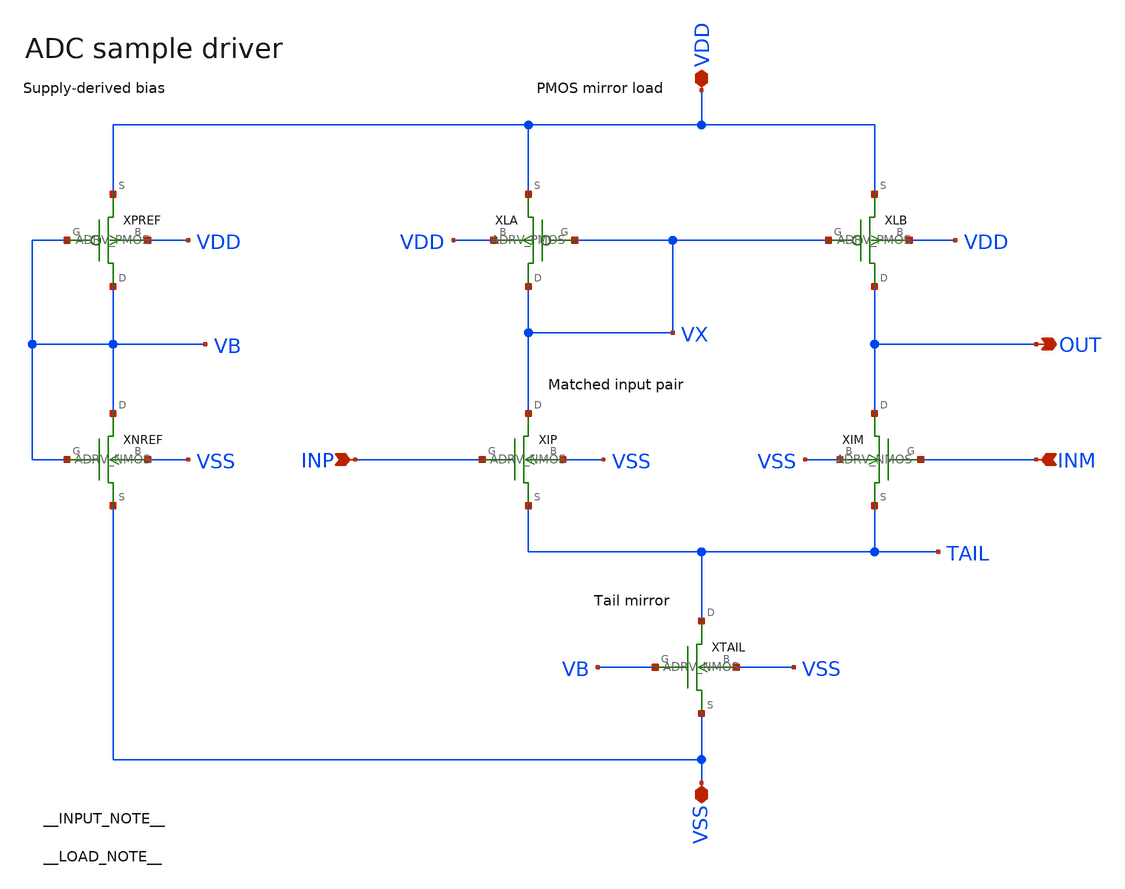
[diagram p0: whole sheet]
** sch_path: examples/sky130-adc-driver/ADRV_OTA.sch
**.subckt ADRV_OTA VDD VSS INP INM OUT
*.iopin VDD
*.iopin VSS
*.ipin INP
*.ipin INM
*.opin OUT
XPREF VB VB VDD VDD sky130_fd_pr__pfet_01v8 w=1 l=1 nf=1 ad=0.3 as=0.3 pd=2.6 ps=2.6 m=1
XNREF VB VB VSS VSS sky130_fd_pr__nfet_01v8 w=1 l=1 nf=1 ad=0.3 as=0.3 pd=2.6 ps=2.6 m=1
XLA VX VX VDD VDD sky130_fd_pr__pfet_01v8 w=1 l=1 nf=1 ad=0.3 as=0.3 pd=2.6 ps=2.6 m=1
XLB OUT VX VDD VDD sky130_fd_pr__pfet_01v8 w=1 l=1 nf=1 ad=0.3 as=0.3 pd=2.6 ps=2.6 m=1
XIP VX INP TAIL VSS sky130_fd_pr__nfet_01v8 w=1 l=1 nf=1 ad=0.3 as=0.3 pd=2.6 ps=2.6 m=1
XIM OUT INM TAIL VSS sky130_fd_pr__nfet_01v8 w=1 l=1 nf=1 ad=0.3 as=0.3 pd=2.6 ps=2.6 m=1
XTAIL TAIL VB VSS VSS sky130_fd_pr__nfet_01v8 w=1 l=1 nf=1 ad=0.3 as=0.3 pd=2.6 ps=2.6 m=1
**.ends
.end
